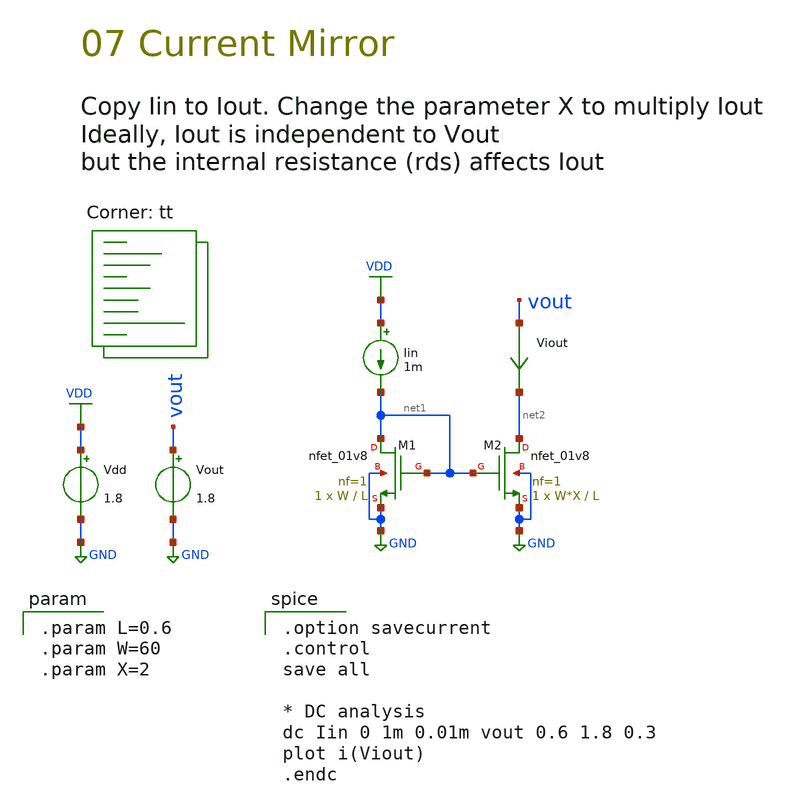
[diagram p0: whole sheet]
** sch_path: 07-a_current-mirror.sch
**.subckt 07-a_current-mirror
Vdd VDD GND 1.8
XM1 net1 net1 GND GND sky130_fd_pr__nfet_01v8 L=L W=W nf=1 ad='int((1 + 1)/2) * W / 1 * 0.29' as='int((1 + 2)/2) * W / 1 * 0.29'
+ pd='2*int((1 + 1)/2) * (W / 1 + 0.29)' ps='2*int((1 + 2)/2) * (W / 1 + 0.29)' nrd='0.29 / W ' nrs='0.29 / W '
+ sa=0 sb=0 sd=0 mult=1 m=1
Viout vout net2 0
.save i(viout)
XM2 net2 net1 GND GND sky130_fd_pr__nfet_01v8 L=L W=W*X nf=1 ad='int((1 + 1)/2) * W*X / 1 * 0.29' as='int((1 + 2)/2) * W*X / 1 * 0.29'
+ pd='2*int((1 + 1)/2) * (W*X / 1 + 0.29)' ps='2*int((1 + 2)/2) * (W*X / 1 + 0.29)' nrd='0.29 / W*X ' nrs='0.29 / W*X '
+ sa=0 sb=0 sd=0 mult=1 m=1
Iin VDD net1 1m
Vout vout GND 1.8
**** begin user architecture code
.lib $::SKYWATER_MODELS/sky130.lib.spice tt

.param L=0.6
.param W=60
.param X=2


.option savecurrent
.control
save all

* DC analysis
dc Iin 0 1m 0.01m vout 0.6 1.8 0.3
plot i(Viout)
.endc

**** end user architecture code
**.ends
.GLOBAL GND
.GLOBAL VDD
.end
